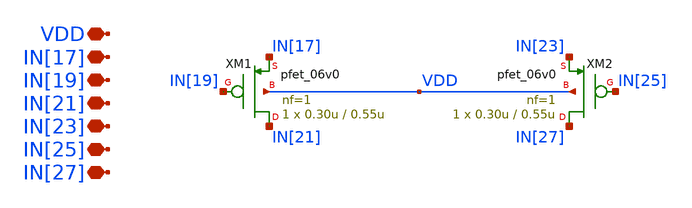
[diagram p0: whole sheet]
** sch_path: designs/libs/core_single-fet/pfet-vdd/pfet-vdd.sch
**.subckt pfet-vdd VDD IN[17] IN[19] IN[21] IN[23] IN[25] IN[27]
*.iopin VDD
*.iopin IN[17]
*.iopin IN[19]
*.iopin IN[21]
*.iopin IN[23]
*.iopin IN[25]
*.iopin IN[27]
XM1 IN[21] IN[19] IN[17] VDD pfet_06v0 L=0.55u W=0.30u nf=1 ad='int((nf+1)/2) * W/nf * 0.18u' as='int((nf+2)/2) * W/nf * 0.18u'
+ pd='2*int((nf+1)/2) * (W/nf + 0.18u)' ps='2*int((nf+2)/2) * (W/nf + 0.18u)' nrd='0.18u / W' nrs='0.18u / W'
+ sa=0 sb=0 sd=0 m=1
XM2 IN[27] IN[25] IN[23] VDD pfet_06v0 L=0.55u W=0.30u nf=1 ad='int((nf+1)/2) * W/nf * 0.18u' as='int((nf+2)/2) * W/nf * 0.18u'
+ pd='2*int((nf+1)/2) * (W/nf + 0.18u)' ps='2*int((nf+2)/2) * (W/nf + 0.18u)' nrd='0.18u / W' nrs='0.18u / W'
+ sa=0 sb=0 sd=0 m=1
**.ends
.end
